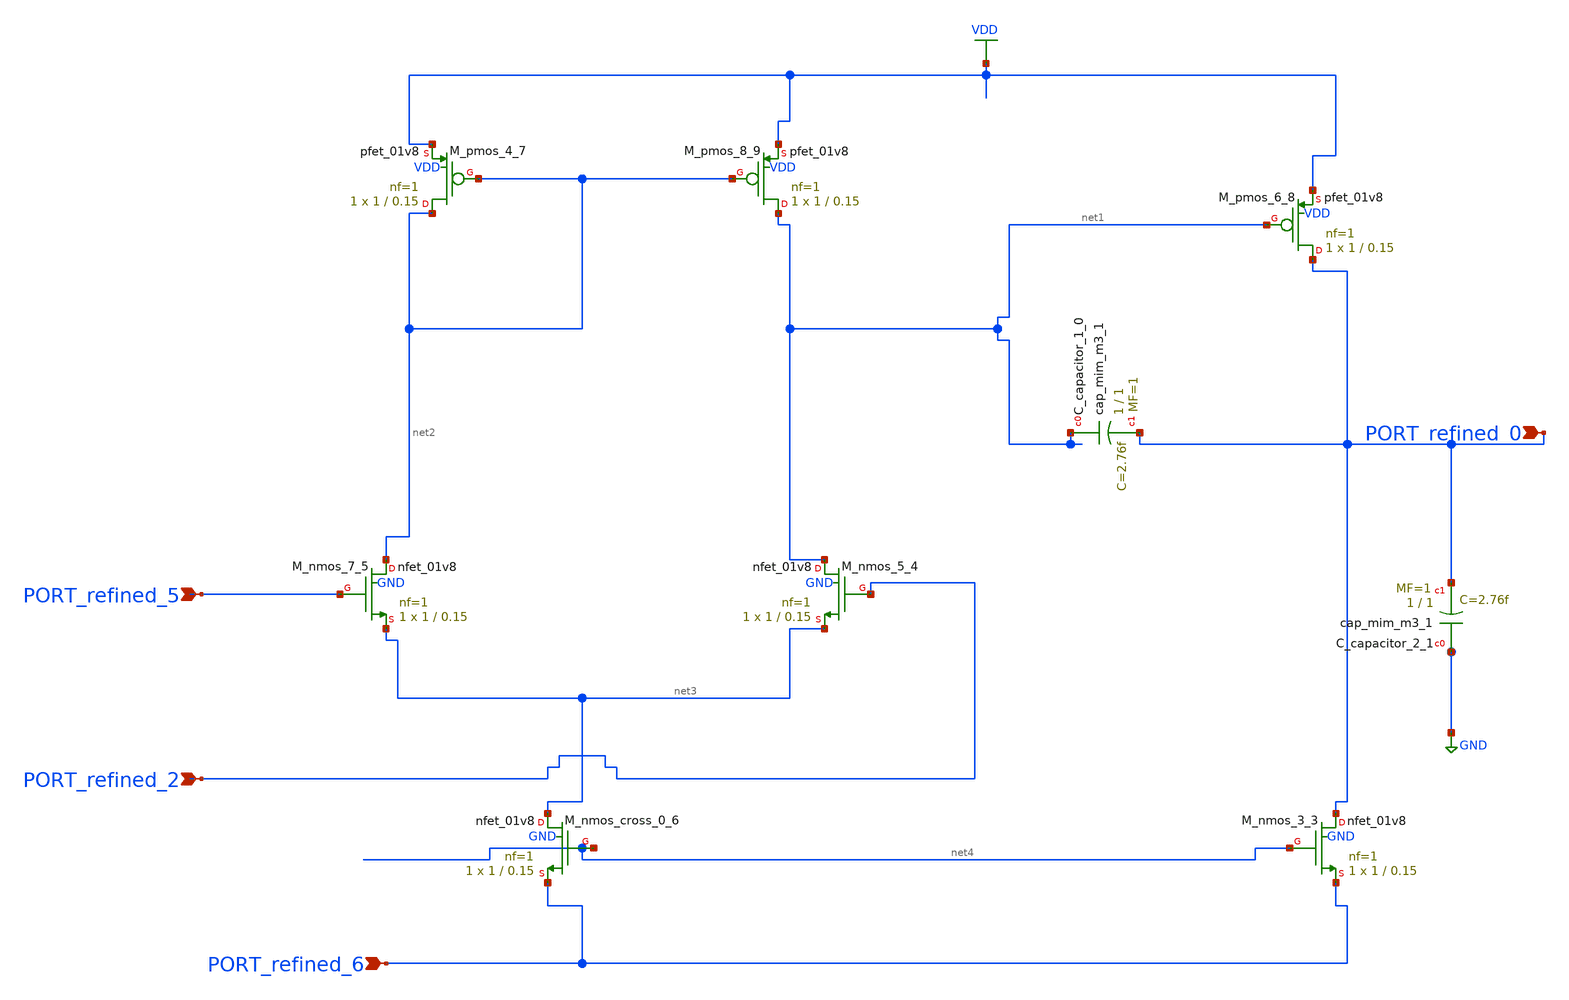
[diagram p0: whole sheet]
** sch_path: schematics/Image2Net/076.sch
**.subckt 076 PORT_refined_5 PORT_refined_0 PORT_refined_2 PORT_refined_6
*.ipin PORT_refined_5
*.ipin PORT_refined_0
*.ipin PORT_refined_2
*.ipin PORT_refined_6
XC_capacitor_1_0 net1 PORT_refined_0 sky130_fd_pr__cap_mim_m3_1 W=1 L=1 MF=1 m=1
XC_capacitor_2_1 GND PORT_refined_0 sky130_fd_pr__cap_mim_m3_1 W=1 L=1 MF=1 m=1
XM_nmos_3_3 PORT_refined_0 net4 PORT_refined_6 GND sky130_fd_pr__nfet_01v8 L=0.15 W=1 nf=1 ad='int((1 + 1)/2) * 1 / 1 * 0.29'
+ as='int((1 + 2)/2) * 1 / 1 * 0.29' pd='2*int((1 + 1)/2) * (1 / 1 + 0.29)' ps='2*int((1 + 2)/2) * (1 / 1 + 0.29)'
+ nrd='0.29 / 1 ' nrs='0.29 / 1 ' sa=0 sb=0 sd=0 mult=1 m=1
XM_nmos_5_4 net1 PORT_refined_2 net3 GND sky130_fd_pr__nfet_01v8 L=0.15 W=1 nf=1 ad='int((1 + 1)/2) * 1 / 1 * 0.29'
+ as='int((1 + 2)/2) * 1 / 1 * 0.29' pd='2*int((1 + 1)/2) * (1 / 1 + 0.29)' ps='2*int((1 + 2)/2) * (1 / 1 + 0.29)'
+ nrd='0.29 / 1 ' nrs='0.29 / 1 ' sa=0 sb=0 sd=0 mult=1 m=1
XM_nmos_7_5 net2 PORT_refined_5 net3 GND sky130_fd_pr__nfet_01v8 L=0.15 W=1 nf=1 ad='int((1 + 1)/2) * 1 / 1 * 0.29'
+ as='int((1 + 2)/2) * 1 / 1 * 0.29' pd='2*int((1 + 1)/2) * (1 / 1 + 0.29)' ps='2*int((1 + 2)/2) * (1 / 1 + 0.29)'
+ nrd='0.29 / 1 ' nrs='0.29 / 1 ' sa=0 sb=0 sd=0 mult=1 m=1
XM_nmos_cross_0_6 net3 net4 PORT_refined_6 GND sky130_fd_pr__nfet_01v8 L=0.15 W=1 nf=1 ad='int((1 + 1)/2) * 1 / 1 * 0.29'
+ as='int((1 + 2)/2) * 1 / 1 * 0.29' pd='2*int((1 + 1)/2) * (1 / 1 + 0.29)' ps='2*int((1 + 2)/2) * (1 / 1 + 0.29)'
+ nrd='0.29 / 1 ' nrs='0.29 / 1 ' sa=0 sb=0 sd=0 mult=1 m=1
XM_pmos_4_7 net2 net2 VDD VDD sky130_fd_pr__pfet_01v8 L=0.15 W=1 nf=1 ad='int((1 + 1)/2) * 1 / 1 * 0.29'
+ as='int((1 + 2)/2) * 1 / 1 * 0.29' pd='2*int((1 + 1)/2) * (1 / 1 + 0.29)' ps='2*int((1 + 2)/2) * (1 / 1 + 0.29)'
+ nrd='0.29 / 1 ' nrs='0.29 / 1 ' sa=0 sb=0 sd=0 mult=1 m=1
XM_pmos_6_8 PORT_refined_0 net1 VDD VDD sky130_fd_pr__pfet_01v8 L=0.15 W=1 nf=1 ad='int((1 + 1)/2) * 1 / 1 * 0.29'
+ as='int((1 + 2)/2) * 1 / 1 * 0.29' pd='2*int((1 + 1)/2) * (1 / 1 + 0.29)' ps='2*int((1 + 2)/2) * (1 / 1 + 0.29)'
+ nrd='0.29 / 1 ' nrs='0.29 / 1 ' sa=0 sb=0 sd=0 mult=1 m=1
XM_pmos_8_9 net1 net2 VDD VDD sky130_fd_pr__pfet_01v8 L=0.15 W=1 nf=1 ad='int((1 + 1)/2) * 1 / 1 * 0.29'
+ as='int((1 + 2)/2) * 1 / 1 * 0.29' pd='2*int((1 + 1)/2) * (1 / 1 + 0.29)' ps='2*int((1 + 2)/2) * (1 / 1 + 0.29)'
+ nrd='0.29 / 1 ' nrs='0.29 / 1 ' sa=0 sb=0 sd=0 mult=1 m=1
**.ends
.GLOBAL GND
.GLOBAL VDD
.end
